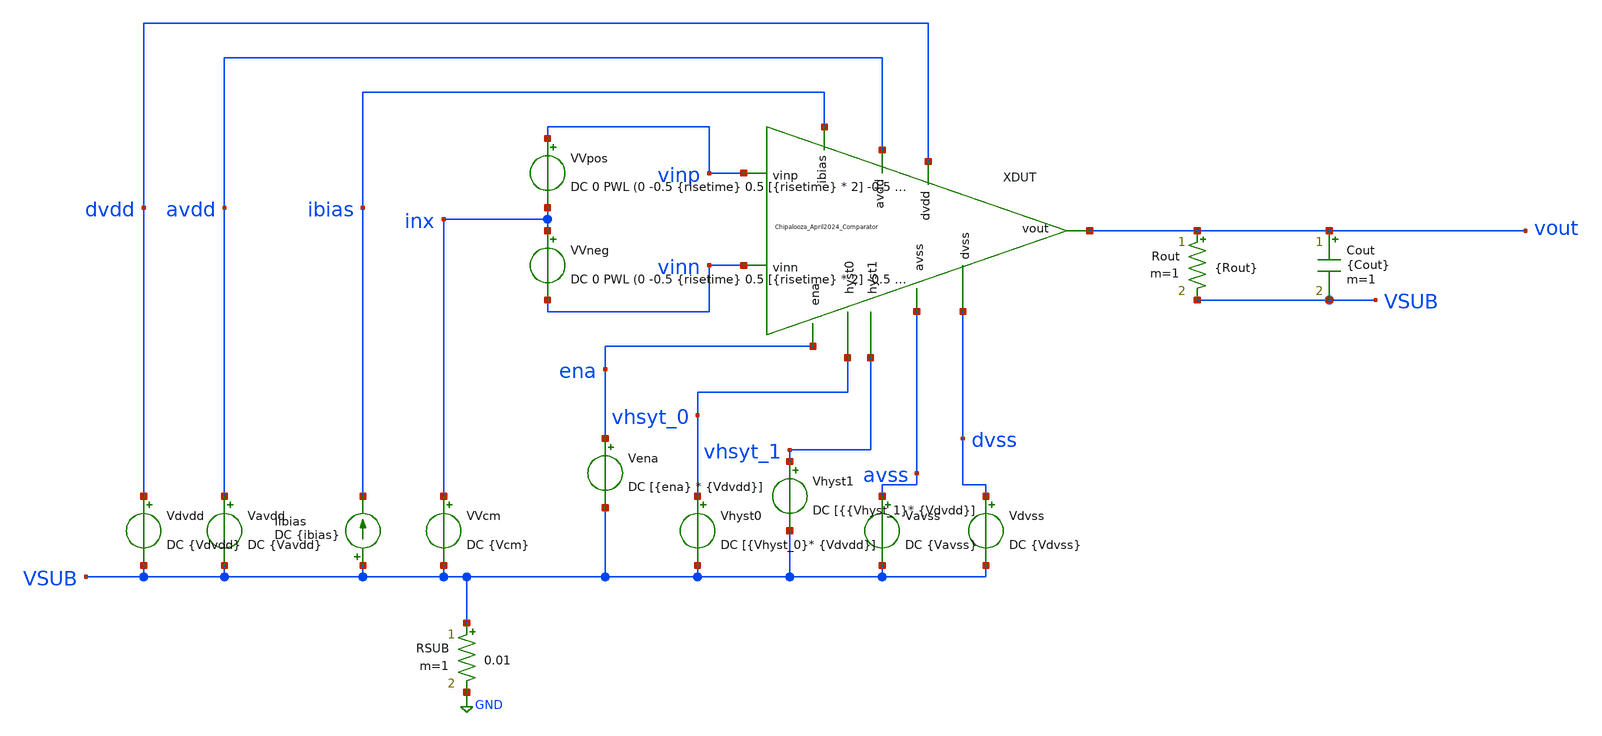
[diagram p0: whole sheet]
** sch_path: Chipalooza_April2024_Comparator/cace/input_offset.sch
**.subckt input_offset
Vavdd avdd VSUB DC {Vavdd}
Rout vout VSUB {Rout} m=1
Cout vout VSUB {Cout} m=1
Vdvdd dvdd VSUB DC {Vdvdd}
Vena ena VSUB DC [{ena} * {Vdvdd}]
Vhyst0 vhsyt_0 VSUB DC [{Vhyst_0}* {Vdvdd}]
Vhyst1 vhsyt_1 VSUB DC [{{Vhyst_1}* {Vdvdd}]
Vavss avss VSUB DC {Vavss}
Vdvss dvss VSUB DC {Vdvss}
RSUB VSUB GND 0.01 m=1
Iibias VSUB ibias DC {ibias}
XDUT vhsyt_0 vhsyt_1 avdd vinp avss vinn dvdd dvss vout ibias ena Chipalooza_April2024_Comparator
VVpos vinp inx DC 0 PWL (0 -0.5 {risetime} 0.5 [{risetime} * 2] -0.5 [{risetime} * 3] 0.5 [{risetime} * 4] -0.5 )
VVneg inx vinn DC 0 PWL (0 -0.5 {risetime} 0.5 [{risetime} * 2] -0.5 [{risetime} * 3] 0.5 [{risetime} * 4] -0.5 )
VVcm inx VSUB DC {Vcm}
**** begin user architecture code

* CACE gensim simulation file {filename}_{N}
* Generated by CACE gensim, Efabless Corporation (c) 2023
* Find the current through the amplifier under condition of static input

.include {DUT_path}

.lib {PDK_ROOT}/{PDK}/libs.tech/combined/sky130.lib.spice {corner}

.option TEMP={temperature}
* Flag unsafe operating conditions (exceeds models' specified limits)
.option warn=1
.option savecurrents
.option save all



.control
** Find zero crossing for positive input differential, zero crossing for negative
** input differential, then compute the average
tran [{risetime} * 2 / 1000] [{risetime} * 2]
meas tran vhigh FIND V(inp) WHEN V(out) = [{Vvdd} / 2] CROSS=1
meas tran vlow FIND V(inp) WHEN V(out) = [{Vvdd} / 2] CROSS=2
let vrise = $&vhigh - {Vcm}
let vfall = $&vlow - {Vcm}

let voffset = 0.5 * ($&vrise + $&vfall)
let vhyst = $&vrise - $&vfall

echo $&voffset $&vhyst > {simpath}/{filename}_{N}.data
*set wr_singlescale
*wrdata {simpath}/{filename}_{N}.data V(out) V(inp) V(inm)

write ngspice/input_offset.raw

quit
.endc


**** end user architecture code
**.ends
.GLOBAL GND
.end
